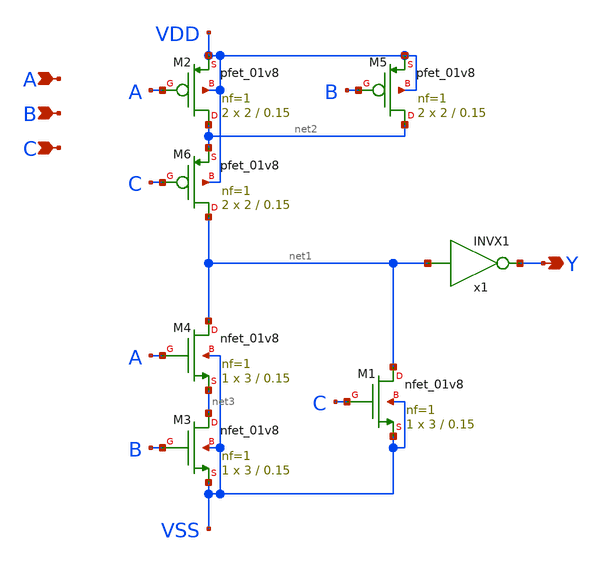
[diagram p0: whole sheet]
** sch_path: lib/xschem/AO3X1.sch
**.subckt AO3X1 Y A B C
*.opin Y
*.ipin A
*.ipin B
*.ipin C
XM1 net1 C VSS VSS sky130_fd_pr__nfet_01v8 L=0.15 W=3 nf=1 ad='int((nf+1)/2) * W/nf * 0.29' as='int((nf+2)/2) * W/nf * 0.29'
+ pd='2*int((nf+1)/2) * (W/nf + 0.29)' ps='2*int((nf+2)/2) * (W/nf + 0.29)' nrd='0.29 / W' nrs='0.29 / W'
+ sa=0 sb=0 sd=0 mult=1 m=1
XM2 net2 A VDD VDD sky130_fd_pr__pfet_01v8 L=0.15 W=2 nf=1 ad='int((nf+1)/2) * W/nf * 0.29' as='int((nf+2)/2) * W/nf * 0.29'
+ pd='2*int((nf+1)/2) * (W/nf + 0.29)' ps='2*int((nf+2)/2) * (W/nf + 0.29)' nrd='0.29 / W' nrs='0.29 / W'
+ sa=0 sb=0 sd=0 mult=2 m=2
XM3 net3 B VSS VSS sky130_fd_pr__nfet_01v8 L=0.15 W=3 nf=1 ad='int((nf+1)/2) * W/nf * 0.29' as='int((nf+2)/2) * W/nf * 0.29'
+ pd='2*int((nf+1)/2) * (W/nf + 0.29)' ps='2*int((nf+2)/2) * (W/nf + 0.29)' nrd='0.29 / W' nrs='0.29 / W'
+ sa=0 sb=0 sd=0 mult=1 m=1
XM4 net1 A net3 VSS sky130_fd_pr__nfet_01v8 L=0.15 W=3 nf=1 ad='int((nf+1)/2) * W/nf * 0.29' as='int((nf+2)/2) * W/nf * 0.29'
+ pd='2*int((nf+1)/2) * (W/nf + 0.29)' ps='2*int((nf+2)/2) * (W/nf + 0.29)' nrd='0.29 / W' nrs='0.29 / W'
+ sa=0 sb=0 sd=0 mult=1 m=1
XM5 net2 B VDD VDD sky130_fd_pr__pfet_01v8 L=0.15 W=2 nf=1 ad='int((nf+1)/2) * W/nf * 0.29' as='int((nf+2)/2) * W/nf * 0.29'
+ pd='2*int((nf+1)/2) * (W/nf + 0.29)' ps='2*int((nf+2)/2) * (W/nf + 0.29)' nrd='0.29 / W' nrs='0.29 / W'
+ sa=0 sb=0 sd=0 mult=2 m=2
XM6 net1 C net2 VDD sky130_fd_pr__pfet_01v8 L=0.15 W=2 nf=1 ad='int((nf+1)/2) * W/nf * 0.29' as='int((nf+2)/2) * W/nf * 0.29'
+ pd='2*int((nf+1)/2) * (W/nf + 0.29)' ps='2*int((nf+2)/2) * (W/nf + 0.29)' nrd='0.29 / W' nrs='0.29 / W'
+ sa=0 sb=0 sd=0 mult=2 m=2
x1 Y net1 INVX1
**.ends
.end
